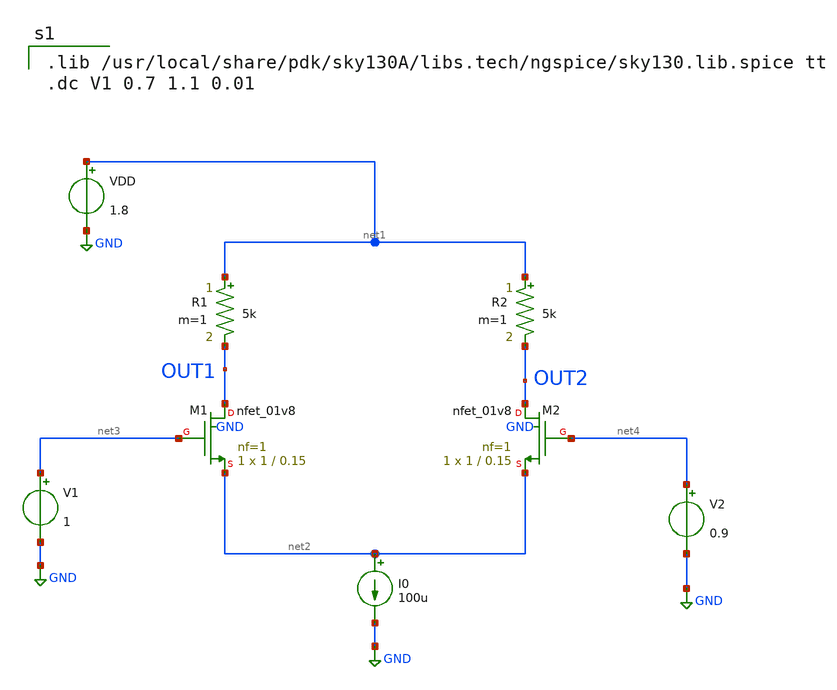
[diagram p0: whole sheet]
** sch_path: Differential_Pair/differential_pair.sch
**.subckt differential_pair
XM1 OUT1 net3 net2 GND sky130_fd_pr__nfet_01v8 L=0.15 W=1 nf=1 ad='int((1 + 1)/2) * 1 / 1 * 0.29' as='int((1 + 2)/2) * 1 / 1 * 0.29'
+ pd='2*int((1 + 1)/2) * (1 / 1 + 0.29)' ps='2*int((1 + 2)/2) * (1 / 1 + 0.29)' nrd='0.29 / 1 ' nrs='0.29 / 1 '
+ sa=0 sb=0 sd=0 mult=1 m=1
XM2 OUT2 net4 net2 GND sky130_fd_pr__nfet_01v8 L=0.15 W=1 nf=1 ad='int((1 + 1)/2) * 1 / 1 * 0.29' as='int((1 + 2)/2) * 1 / 1 * 0.29'
+ pd='2*int((1 + 1)/2) * (1 / 1 + 0.29)' ps='2*int((1 + 2)/2) * (1 / 1 + 0.29)' nrd='0.29 / 1 ' nrs='0.29 / 1 '
+ sa=0 sb=0 sd=0 mult=1 m=1
R1 net1 OUT1 5k m=1
R2 net1 OUT2 5k m=1
I0 net2 GND 100u
V1 net3 GND 1
V2 net4 GND 0.9
VDD net1 GND 1.8
**** begin user architecture code

.lib /usr/local/share/pdk/sky130A/libs.tech/ngspice/sky130.lib.spice tt
.dc V1 0.7 1.1 0.01

**** end user architecture code
**.ends
.GLOBAL GND
.end
